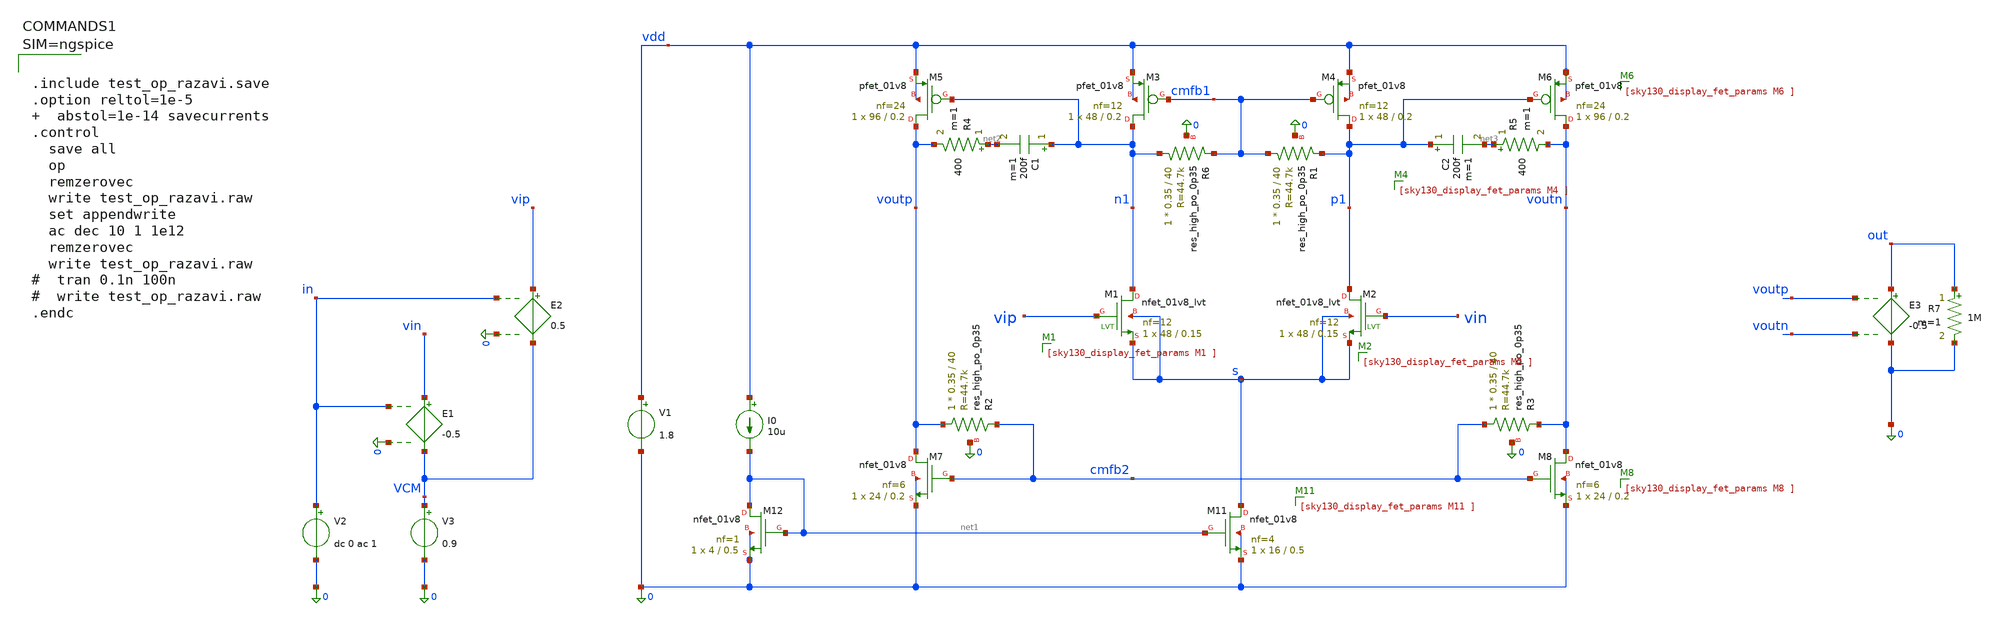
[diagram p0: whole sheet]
** sch_path: test_op_razavi.sch
**.subckt test_op_razavi
XM1 n1 vip s s sky130_fd_pr__nfet_01v8_lvt L=0.15 W=48 nf=12 ad='int((12 + 1)/2) * 48 / 12 * 0.29' as='int((12 + 2)/2) * 48 / 12 * 0.29'
+ pd='2*int((12 + 1)/2) * (48 / 12 + 0.29)' ps='2*int((12 + 2)/2) * (48 / 12 + 0.29)' nrd='0.29 / 48 '
+ nrs='0.29 / 48 ' sa=0 sb=0 sd=0 mult=1 m=1
XM2 p1 vin s s sky130_fd_pr__nfet_01v8_lvt L=0.15 W=48 nf=12 ad='int((12 + 1)/2) * 48 / 12 * 0.29' as='int((12 + 2)/2) * 48 / 12 * 0.29'
+ pd='2*int((12 + 1)/2) * (48 / 12 + 0.29)' ps='2*int((12 + 2)/2) * (48 / 12 + 0.29)' nrd='0.29 / 48 '
+ nrs='0.29 / 48 ' sa=0 sb=0 sd=0 mult=1 m=1
XM7 voutp cmfb2 0 0 sky130_fd_pr__nfet_01v8 L=0.2 W=24 nf=6 ad='int((6 + 1)/2) * 24 / 6 * 0.29' as='int((6 + 2)/2) * 24 / 6 * 0.29'
+ pd='2*int((6 + 1)/2) * (24 / 6 + 0.29)' ps='2*int((6 + 2)/2) * (24 / 6 + 0.29)' nrd='0.29 / 24 ' nrs='0.29 / 24 '
+ sa=0 sb=0 sd=0 mult=1 m=1
XM8 voutn cmfb2 0 0 sky130_fd_pr__nfet_01v8 L=0.2 W=24 nf=6 ad='int((6 + 1)/2) * 24 / 6 * 0.29' as='int((6 + 2)/2) * 24 / 6 * 0.29'
+ pd='2*int((6 + 1)/2) * (24 / 6 + 0.29)' ps='2*int((6 + 2)/2) * (24 / 6 + 0.29)' nrd='0.29 / 24 ' nrs='0.29 / 24 '
+ sa=0 sb=0 sd=0 mult=1 m=1
XM4 p1 cmfb1 vdd vdd sky130_fd_pr__pfet_01v8 L=0.2 W=48 nf=12 ad='int((nf+1)/2) * W/nf * 0.29' as='int((nf+2)/2) * W/nf * 0.29'
+ pd='2*int((nf+1)/2) * (W/nf + 0.29)' ps='2*int((nf+2)/2) * (W/nf + 0.29)' nrd='0.29 / W' nrs='0.29 / W'
+ sa=0 sb=0 sd=0 mult=1 m=1
XM3 n1 cmfb1 vdd vdd sky130_fd_pr__pfet_01v8 L=0.2 W=48 nf=12 ad='int((nf+1)/2) * W/nf * 0.29' as='int((nf+2)/2) * W/nf * 0.29'
+ pd='2*int((nf+1)/2) * (W/nf + 0.29)' ps='2*int((nf+2)/2) * (W/nf + 0.29)' nrd='0.29 / W' nrs='0.29 / W'
+ sa=0 sb=0 sd=0 mult=1 m=1
XM5 voutp n1 vdd vdd sky130_fd_pr__pfet_01v8 L=0.2 W=96 nf=24 ad='int((nf+1)/2) * W/nf * 0.29' as='int((nf+2)/2) * W/nf * 0.29'
+ pd='2*int((nf+1)/2) * (W/nf + 0.29)' ps='2*int((nf+2)/2) * (W/nf + 0.29)' nrd='0.29 / W' nrs='0.29 / W'
+ sa=0 sb=0 sd=0 mult=1 m=1
XM6 voutn p1 vdd vdd sky130_fd_pr__pfet_01v8 L=0.2 W=96 nf=24 ad='int((nf+1)/2) * W/nf * 0.29' as='int((nf+2)/2) * W/nf * 0.29'
+ pd='2*int((nf+1)/2) * (W/nf + 0.29)' ps='2*int((nf+2)/2) * (W/nf + 0.29)' nrd='0.29 / W' nrs='0.29 / W'
+ sa=0 sb=0 sd=0 mult=1 m=1
XR6 n1 cmfb1 0 sky130_fd_pr__res_high_po_0p35 L=40 mult=1 m=1
XR1 cmfb1 p1 0 sky130_fd_pr__res_high_po_0p35 L=40 mult=1 m=1
XR2 voutp cmfb2 0 sky130_fd_pr__res_high_po_0p35 L=40 mult=1 m=1
XR3 cmfb2 voutn 0 sky130_fd_pr__res_high_po_0p35 L=40 mult=1 m=1
I0 vdd net1 10u
V1 vdd 0 1.8
.save i(v1)
C1 n1 net2 200f m=1
R4 net2 voutp 400 m=1
C2 p1 net3 200f m=1
R5 net3 voutn 400 m=1
V3 VCM 0 0.9
XM11 s net1 0 0 sky130_fd_pr__nfet_01v8 L=0.5 W=16 nf=4 ad='int((4 + 1)/2) * 16 / 4 * 0.29' as='int((4 + 2)/2) * 16 / 4 * 0.29'
+ pd='2*int((4 + 1)/2) * (16 / 4 + 0.29)' ps='2*int((4 + 2)/2) * (16 / 4 + 0.29)' nrd='0.29 / 16 ' nrs='0.29 / 16 '
+ sa=0 sb=0 sd=0 mult=1 m=1
XM12 net1 net1 0 0 sky130_fd_pr__nfet_01v8 L=0.5 W=4 nf=1 ad='int((1 + 1)/2) * 4 / 1 * 0.29' as='int((1 + 2)/2) * 4 / 1 * 0.29'
+ pd='2*int((1 + 1)/2) * (4 / 1 + 0.29)' ps='2*int((1 + 2)/2) * (4 / 1 + 0.29)' nrd='0.29 / 4 ' nrs='0.29 / 4 '
+ sa=0 sb=0 sd=0 mult=1 m=1
E1 vin VCM in 0 -0.5
E2 vip VCM in 0 0.5
V2 in 0 dc 0 ac 1
E3 out 0 voutp voutn -0.5
R7 out 0 1M m=1
**** begin user architecture code

** opencircuitdesign pdks install
.lib $::SKYWATER_MODELS/sky130.lib.spice tt




.include test_op_razavi.save
.option reltol=1e-5   abstol=1e-14 savecurrents
.control
  save all
  op
  remzerovec
  write test_op_razavi.raw
  set appendwrite
  ac dec 10 1 1e12
  remzerovec
  write test_op_razavi.raw
#  tran 0.1n 100n
#  write test_op_razavi.raw
.endc



**** end user architecture code
**.ends
.end
